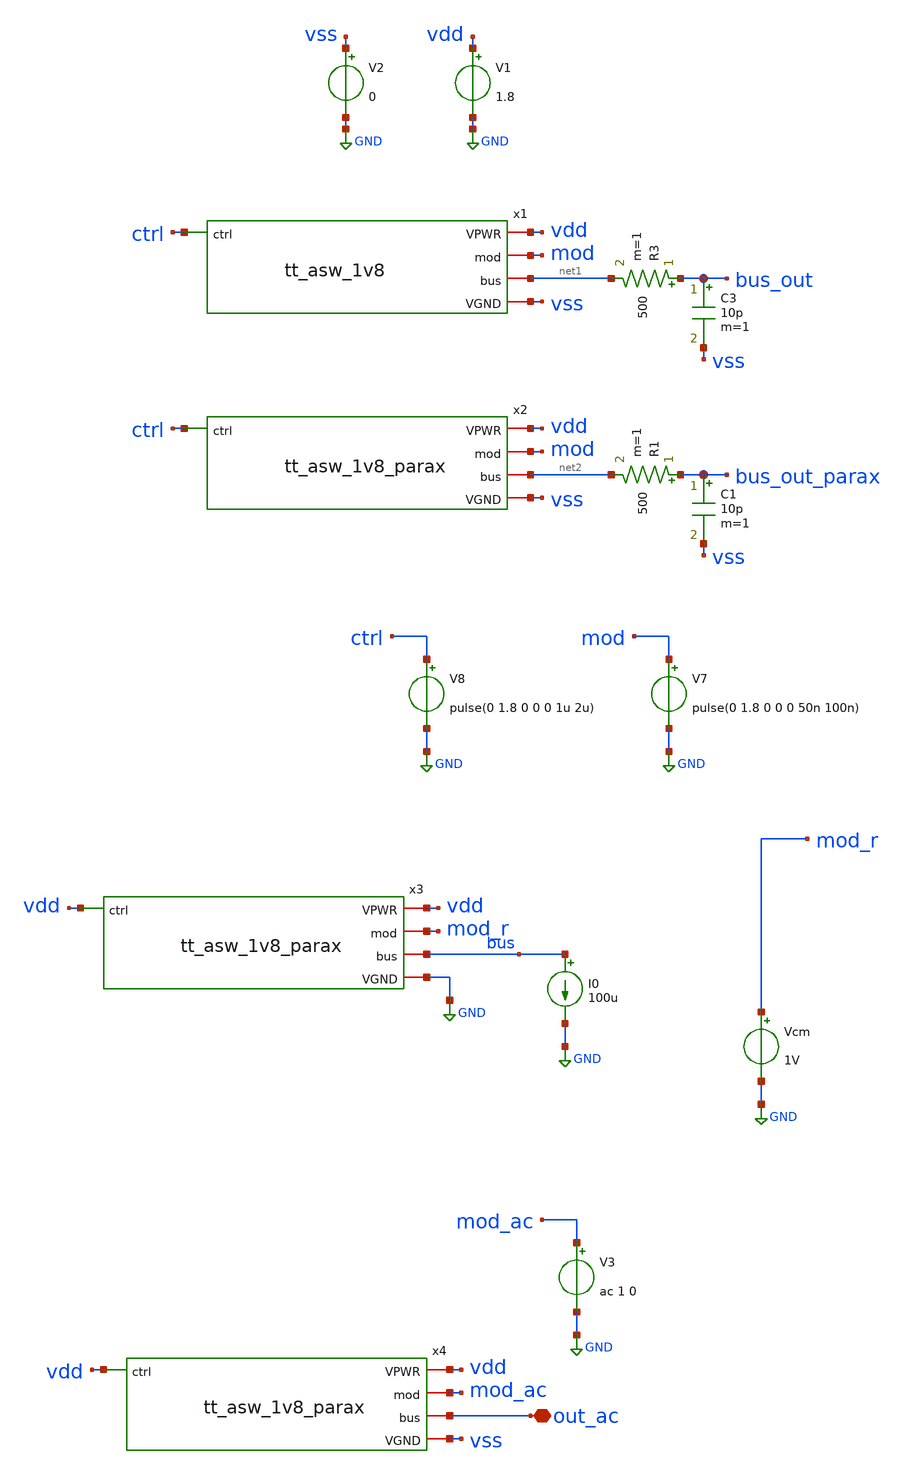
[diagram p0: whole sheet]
** sch_path: asw/tt_asw_1v8/xschem/testbench.sch
**.subckt testbench out_ac
*.iopin out_ac
x1 vss vdd ctrl mod net1 tt_asw_1v8
V1 vdd GND 1.8
R3 bus_out net1 500 m=1
C3 bus_out vss 10p m=1
V2 vss GND 0
V7 mod GND pulse(0 1.8 0 0 0 50n 100n)
V8 ctrl GND pulse(0 1.8 0 0 0 1u 2u)
x2 vss vdd ctrl mod net2 tt_asw_1v8_parax
R1 bus_out_parax net2 500 m=1
C1 bus_out_parax vss 10p m=1
x3 GND vdd vdd mod_r bus tt_asw_1v8_parax
Vcm mod_r GND 1V
I0 bus GND 100u
V3 mod_ac GND ac 1 0
x4 vss vdd vdd mod_ac out_ac tt_asw_1v8_parax
**** begin user architecture code

** opencircuitdesign pdks install
.lib $::SKYWATER_MODELS/sky130.lib.spice tt
.include $::SKYWATER_STDCELLS/sky130_fd_sc_hd.spice





.param mc_mm_switch=0
.control
save all
tran 500p 2u uic
write testbench.raw
reset
save all
dc Vcm 0 1.8 0.01
remzerovec
write testbench_dc.raw

ac dec 10 1 200e6
remzerovec
write testbench_ac.raw

*quit 0
.endc
.end


**** end user architecture code
**.ends

* expanding   symbol:  tt_asw_1v8.sym # of pins=5
** sym_path: asw/sky130/tt_asw_1v8/xschem/tt_asw_1v8.sym
** sch_path: asw/sky130/tt_asw_1v8/xschem/tt_asw_1v8.sch
.subckt tt_asw_1v8 VGND VPWR ctrl mod bus
*.iopin VPWR
*.iopin VGND
*.iopin mod
*.iopin bus
*.ipin ctrl
XM4 tgon tgon_n VGND VGND sky130_fd_pr__nfet_01v8 L=0.15 W=1.5 nf=1 ad='int((nf+1)/2) * W/nf * 0.29'
+ as='int((nf+2)/2) * W/nf * 0.29' pd='2*int((nf+1)/2) * (W/nf + 0.29)' ps='2*int((nf+2)/2) * (W/nf + 0.29)'
+ nrd='0.29 / W' nrs='0.29 / W' sa=0 sb=0 sd=0 mult=1 m=1
XM3 tgon tgon_n VPWR VPWR sky130_fd_pr__pfet_01v8 L=0.15 W=3 nf=2 ad='int((nf+1)/2) * W/nf * 0.29' as='int((nf+2)/2) * W/nf * 0.29'
+ pd='2*int((nf+1)/2) * (W/nf + 0.29)' ps='2*int((nf+2)/2) * (W/nf + 0.29)' nrd='0.29 / W' nrs='0.29 / W'
+ sa=0 sb=0 sd=0 mult=1 m=1
XM2 tgon_n ctrl VGND VGND sky130_fd_pr__nfet_01v8 L=0.15 W=1.5 nf=1 ad='int((nf+1)/2) * W/nf * 0.29'
+ as='int((nf+2)/2) * W/nf * 0.29' pd='2*int((nf+1)/2) * (W/nf + 0.29)' ps='2*int((nf+2)/2) * (W/nf + 0.29)'
+ nrd='0.29 / W' nrs='0.29 / W' sa=0 sb=0 sd=0 mult=1 m=1
XM1 tgon_n ctrl VPWR VPWR sky130_fd_pr__pfet_01v8 L=0.15 W=3 nf=2 ad='int((nf+1)/2) * W/nf * 0.29' as='int((nf+2)/2) * W/nf * 0.29'
+ pd='2*int((nf+1)/2) * (W/nf + 0.29)' ps='2*int((nf+2)/2) * (W/nf + 0.29)' nrd='0.29 / W' nrs='0.29 / W'
+ sa=0 sb=0 sd=0 mult=1 m=1
XM6 bus tgon mod VGND sky130_fd_pr__nfet_01v8_lvt L=0.35 W=31.5 nf=7 ad='int((nf+1)/2) * W/nf * 0.29'
+ as='int((nf+2)/2) * W/nf * 0.29' pd='2*int((nf+1)/2) * (W/nf + 0.29)' ps='2*int((nf+2)/2) * (W/nf + 0.29)'
+ nrd='0.29 / W' nrs='0.29 / W' sa=0 sb=0 sd=0 mult=1 m=1
XM5 bus tgon_n mod VPWR sky130_fd_pr__pfet_01v8_lvt L=0.35 W=94.5 nf=21 ad='int((nf+1)/2) * W/nf * 0.29'
+ as='int((nf+2)/2) * W/nf * 0.29' pd='2*int((nf+1)/2) * (W/nf + 0.29)' ps='2*int((nf+2)/2) * (W/nf + 0.29)'
+ nrd='0.29 / W' nrs='0.29 / W' sa=0 sb=0 sd=0 mult=1 m=1
.ends


* expanding   symbol:  tt_asw_1v8_parax.sym # of pins=5
** sym_path: asw/sky130/tt_asw_1v8/xschem/tt_asw_1v8.sym
.include [file normalize ../mag/tt_asw_1v8.sim.spice]
.GLOBAL GND
.end
